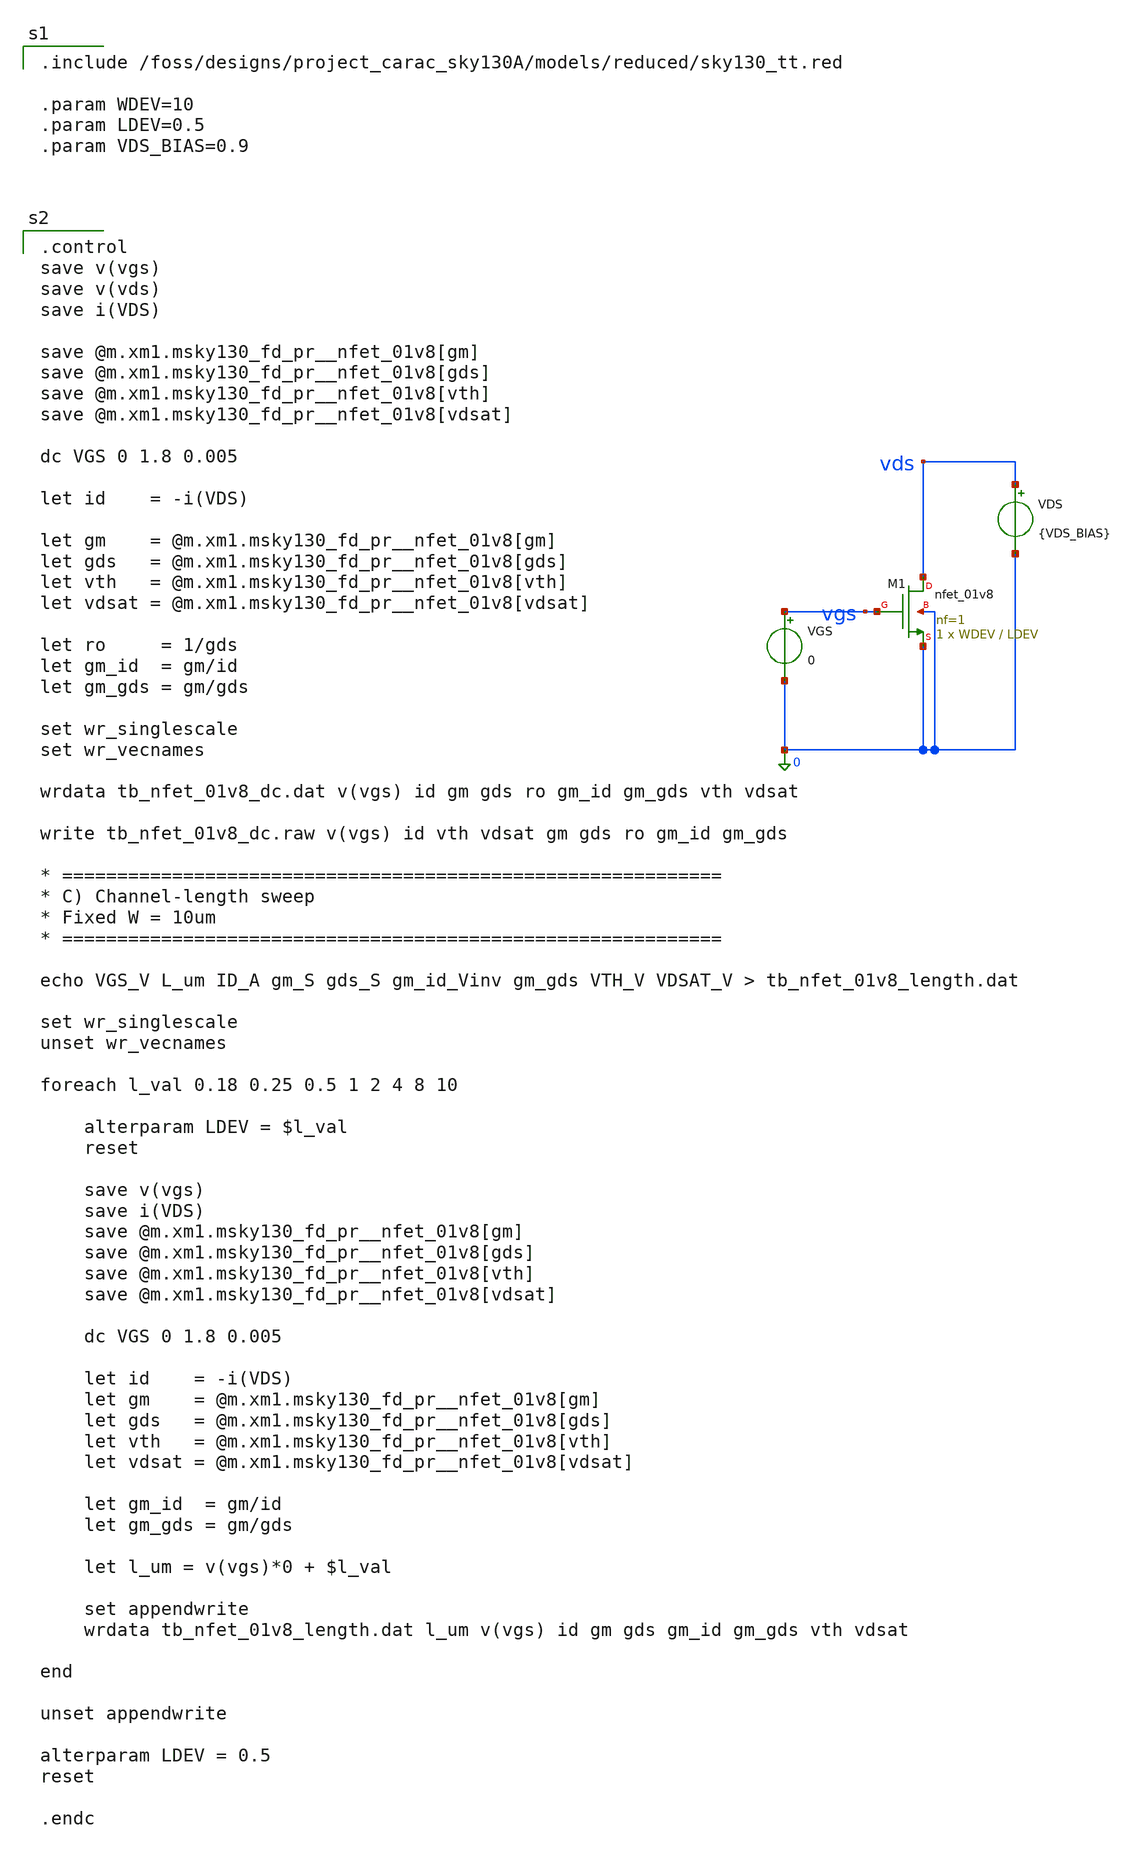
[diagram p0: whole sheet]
** sch_path: dfii/project_carac_sky130A_sim/tb_nfet_01v8_dc.sch
* Copyright 2021 Stefan Frederik Schippers
* Licensed under the Apache License, Version 2.0 (the "License");
* you may not use this file except in compliance with the License.
* You may obtain a copy of the License at
* https://www.apache.org/licenses/LICENSE-2.0
* Unless required by applicable law or agreed to in writing, software
* distributed under the License is distributed on an "AS IS" BASIS,
* WITHOUT WARRANTIES OR CONDITIONS OF ANY KIND, either express or implied.
* See the License for the specific language governing permissions and
* limitations under the License.

.include /foss/designs/project_carac_sky130A/models/reduced/sky130_tt.red

.param WDEV=10
.param LDEV=0.5
.param VDS_BIAS=0.9



**.subckt tb_nfet_01v8_dc
XM1 vds vgs 0 0 sky130_fd_pr__nfet_01v8 L=LDEV W=WDEV nf=1 ad='int((1 + 1)/2) * WDEV / 1 * 0.29' as='int((1 + 2)/2) * WDEV / 1 * 0.29'
+ pd='2*int((1 + 1)/2) * (WDEV / 1 + 0.29)' ps='2*int((1 + 2)/2) * (WDEV / 1 + 0.29)' nrd='0.29 / WDEV '
+ nrs='0.29 / WDEV ' sa=0 sb=0 sd=0 mult=1 m=1
VGS vgs 0 0
VDS vds 0 {VDS_BIAS}
**.ends
**** begin user architecture code

.control
save v(vgs)
save v(vds)
save i(VDS)

save @m.xm1.msky130_fd_pr__nfet_01v8[gm]
save @m.xm1.msky130_fd_pr__nfet_01v8[gds]
save @m.xm1.msky130_fd_pr__nfet_01v8[vth]
save @m.xm1.msky130_fd_pr__nfet_01v8[vdsat]

dc VGS 0 1.8 0.005

let id    = -i(VDS)

let gm    = @m.xm1.msky130_fd_pr__nfet_01v8[gm]
let gds   = @m.xm1.msky130_fd_pr__nfet_01v8[gds]
let vth   = @m.xm1.msky130_fd_pr__nfet_01v8[vth]
let vdsat = @m.xm1.msky130_fd_pr__nfet_01v8[vdsat]

let ro     = 1/gds
let gm_id  = gm/id
let gm_gds = gm/gds

set wr_singlescale
set wr_vecnames

wrdata tb_nfet_01v8_dc.dat v(vgs) id gm gds ro gm_id gm_gds vth vdsat

write tb_nfet_01v8_dc.raw v(vgs) id vth vdsat gm gds ro gm_id gm_gds

* ============================================================
* C) Channel-length sweep
* Fixed W = 10um
* ============================================================

echo VGS_V L_um ID_A gm_S gds_S gm_id_Vinv gm_gds VTH_V VDSAT_V > tb_nfet_01v8_length.dat

set wr_singlescale
unset wr_vecnames

foreach l_val 0.18 0.25 0.5 1 2 4 8 10

    alterparam LDEV = $l_val
    reset

    save v(vgs)
    save i(VDS)
    save @m.xm1.msky130_fd_pr__nfet_01v8[gm]
    save @m.xm1.msky130_fd_pr__nfet_01v8[gds]
    save @m.xm1.msky130_fd_pr__nfet_01v8[vth]
    save @m.xm1.msky130_fd_pr__nfet_01v8[vdsat]

    dc VGS 0 1.8 0.005

    let id    = -i(VDS)
    let gm    = @m.xm1.msky130_fd_pr__nfet_01v8[gm]
    let gds   = @m.xm1.msky130_fd_pr__nfet_01v8[gds]
    let vth   = @m.xm1.msky130_fd_pr__nfet_01v8[vth]
    let vdsat = @m.xm1.msky130_fd_pr__nfet_01v8[vdsat]

    let gm_id  = gm/id
    let gm_gds = gm/gds

    let l_um = v(vgs)*0 + $l_val

    set appendwrite
    wrdata tb_nfet_01v8_length.dat l_um v(vgs) id gm gds gm_id gm_gds vth vdsat

end

unset appendwrite

alterparam LDEV = 0.5
reset

.endc

**** end user architecture code
.end
